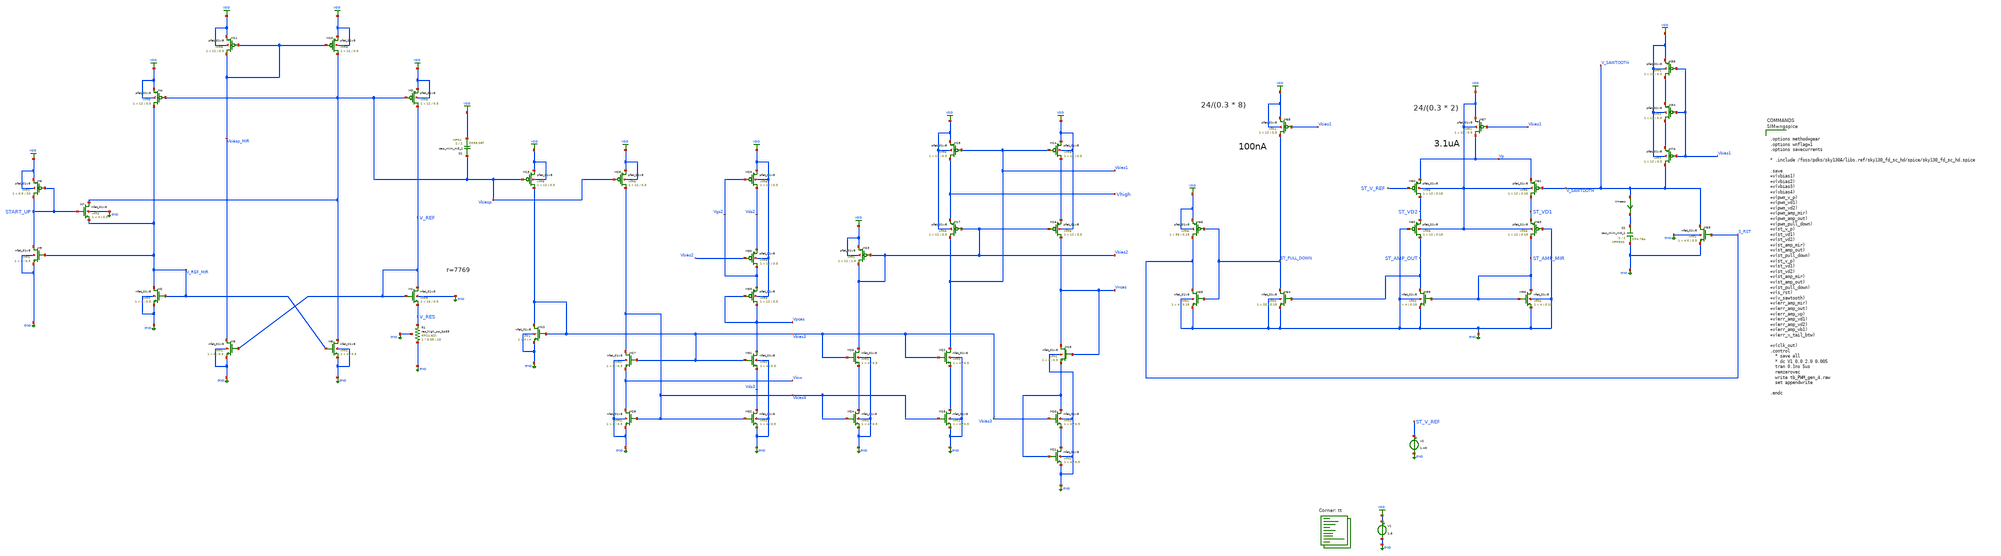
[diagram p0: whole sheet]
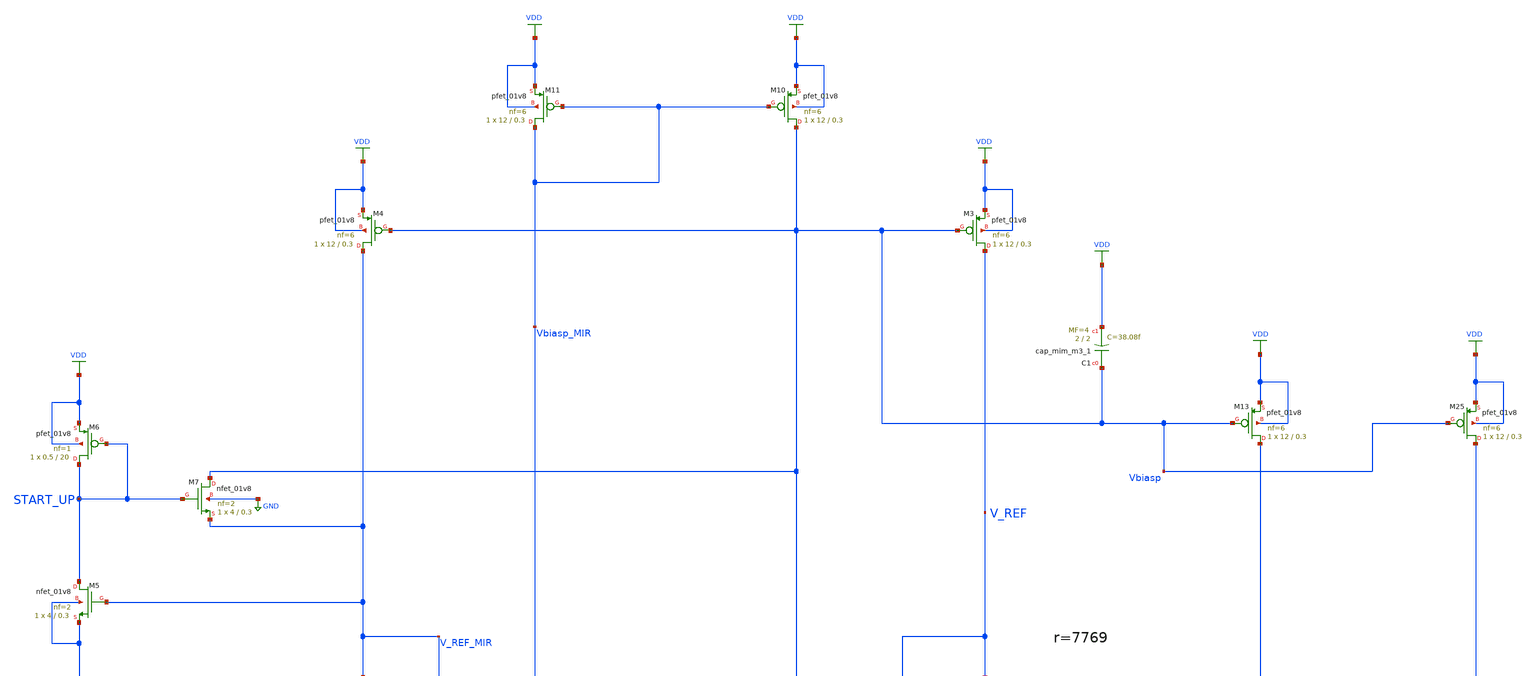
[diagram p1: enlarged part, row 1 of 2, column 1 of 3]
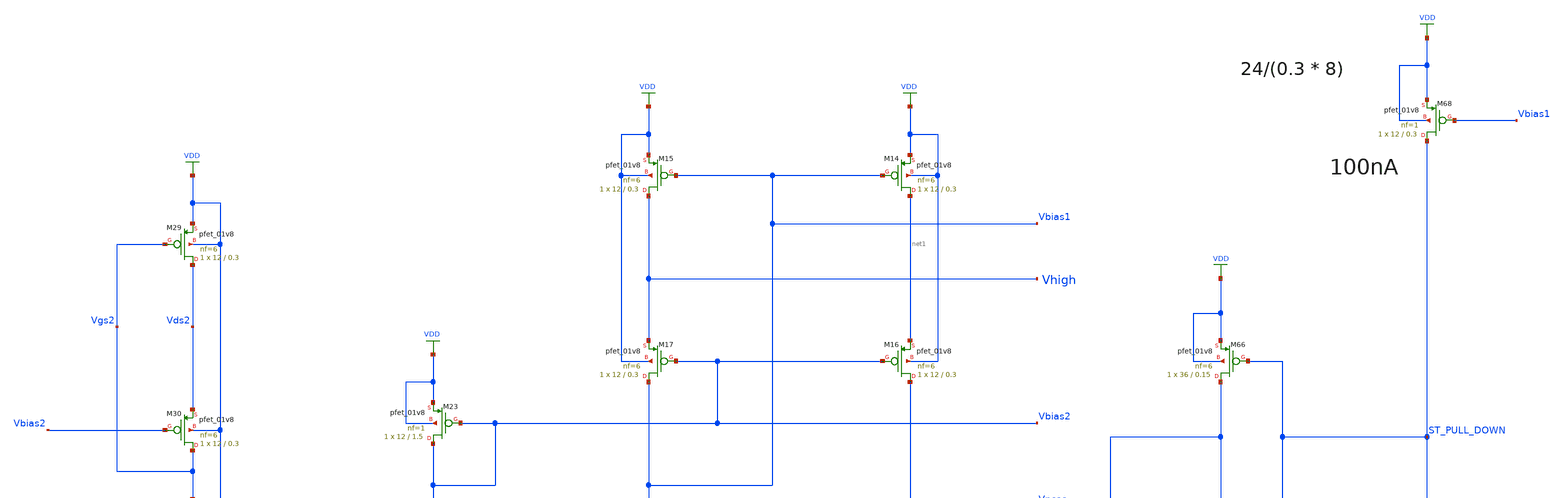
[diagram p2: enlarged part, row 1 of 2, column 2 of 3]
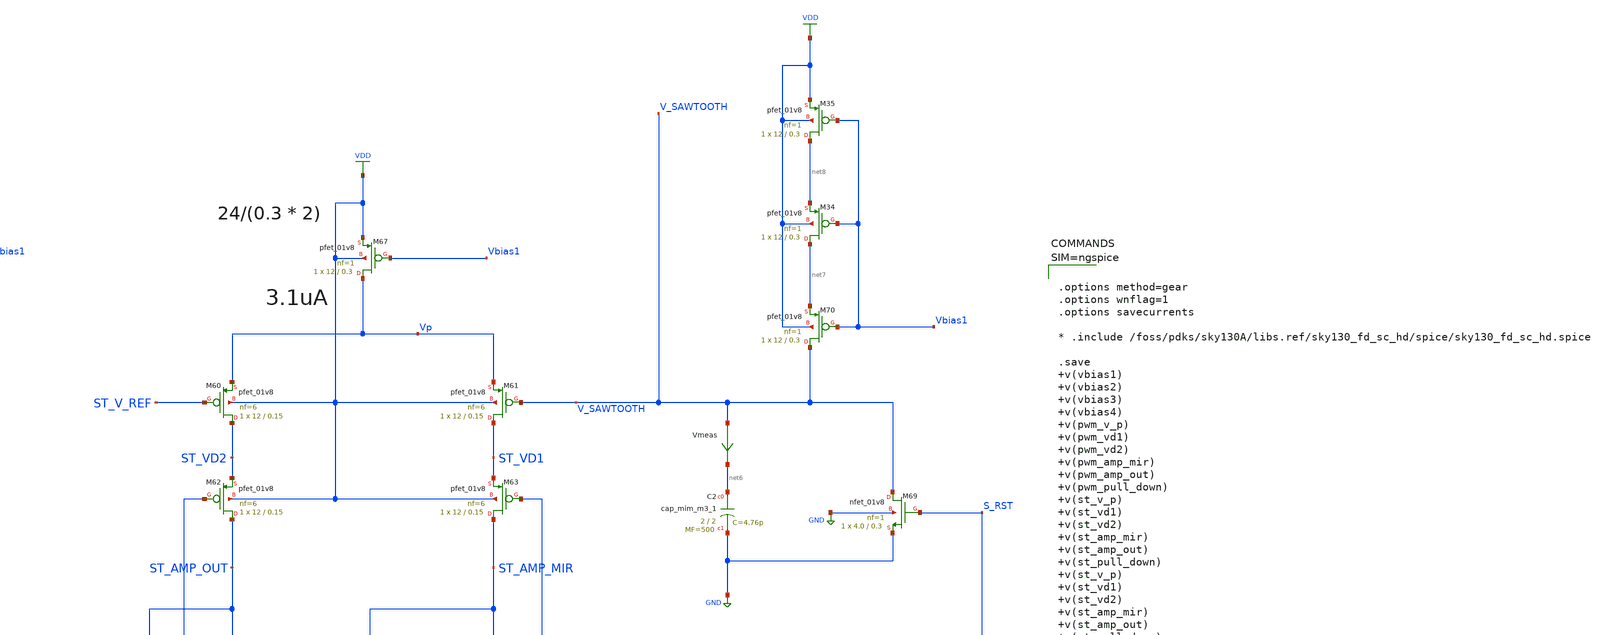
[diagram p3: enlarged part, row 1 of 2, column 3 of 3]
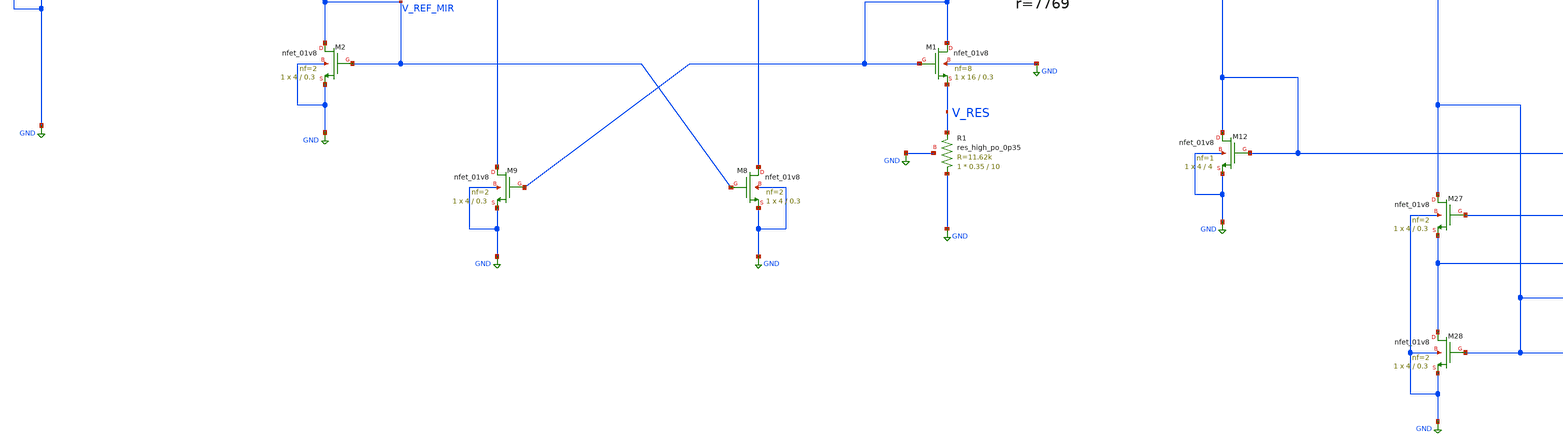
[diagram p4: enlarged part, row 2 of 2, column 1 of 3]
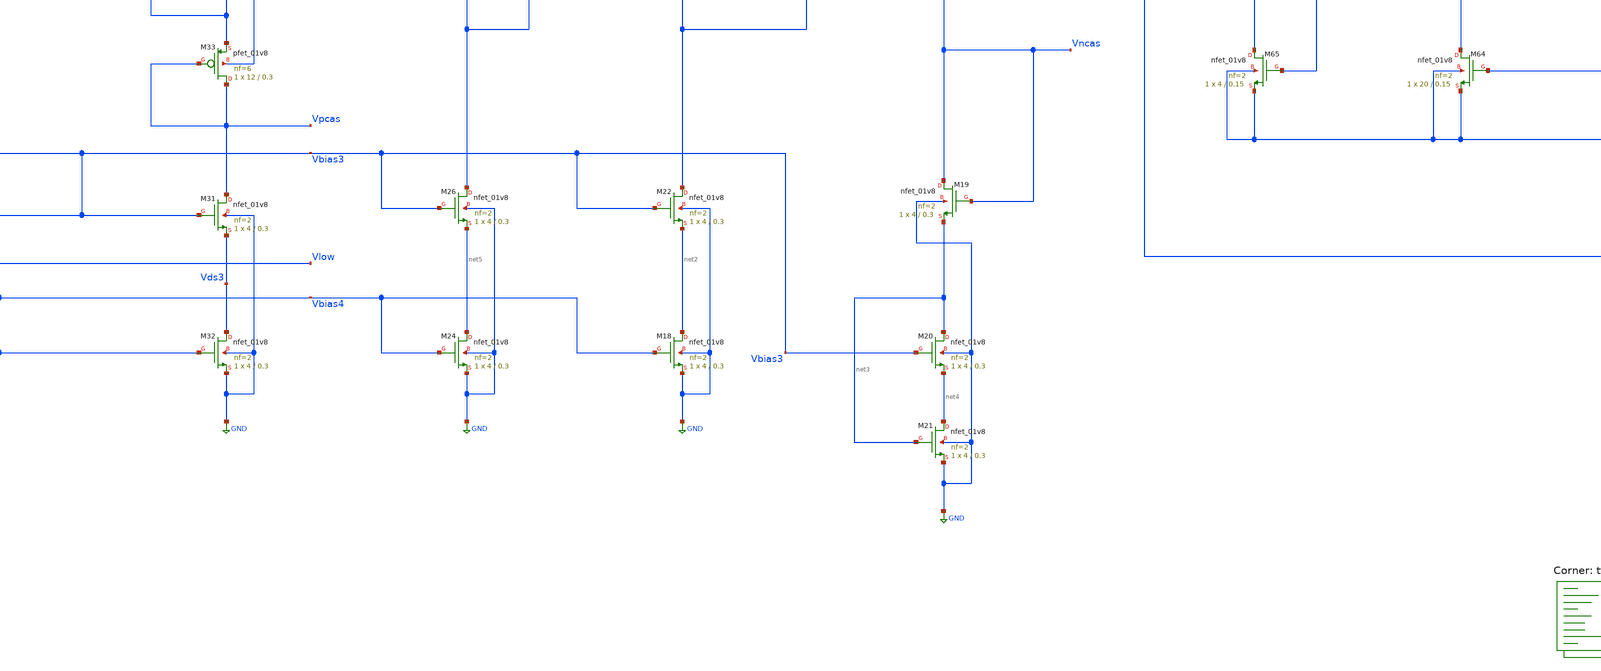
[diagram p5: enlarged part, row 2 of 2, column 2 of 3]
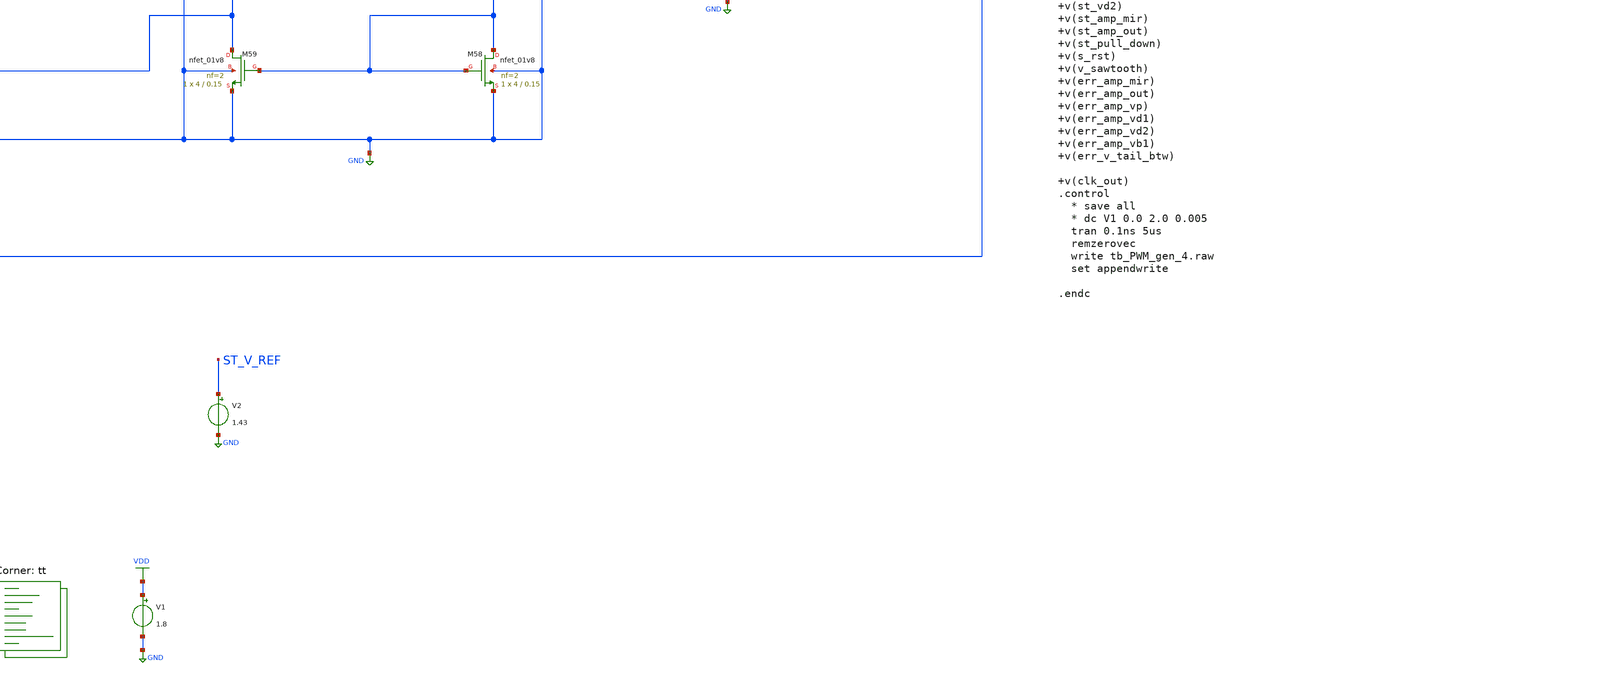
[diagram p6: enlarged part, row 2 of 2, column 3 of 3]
** sch_path: projects/ASU/EEE572/schematic/tb_PWM_gen_4.sch
**.subckt tb_PWM_gen_4
V1 VDD GND 1.8
V2 ST_V_REF GND 1.43
XM1 V_REF V_REF V_RES GND sky130_fd_pr__nfet_01v8 L=0.3 W=16 nf=8 ad='int((nf+1)/2) * W/nf * 0.29' as='int((nf+2)/2) * W/nf * 0.29'
+ pd='2*int((nf+1)/2) * (W/nf + 0.29)' ps='2*int((nf+2)/2) * (W/nf + 0.29)' nrd='0.29 / W' nrs='0.29 / W'
+ sa=0 sb=0 sd=0 mult=1 m=1
XM2 V_REF_MIR V_REF_MIR GND GND sky130_fd_pr__nfet_01v8 L=0.3 W=4 nf=2 ad='int((nf+1)/2) * W/nf * 0.29'
+ as='int((nf+2)/2) * W/nf * 0.29' pd='2*int((nf+1)/2) * (W/nf + 0.29)' ps='2*int((nf+2)/2) * (W/nf + 0.29)'
+ nrd='0.29 / W' nrs='0.29 / W' sa=0 sb=0 sd=0 mult=1 m=1
XM5 START_UP V_REF_MIR GND GND sky130_fd_pr__nfet_01v8 L=0.3 W=4 nf=2 ad='int((nf+1)/2) * W/nf * 0.29'
+ as='int((nf+2)/2) * W/nf * 0.29' pd='2*int((nf+1)/2) * (W/nf + 0.29)' ps='2*int((nf+2)/2) * (W/nf + 0.29)'
+ nrd='0.29 / W' nrs='0.29 / W' sa=0 sb=0 sd=0 mult=1 m=1
XM7 Vbiasp START_UP V_REF_MIR GND sky130_fd_pr__nfet_01v8 L=0.3 W=4 nf=2 ad='int((nf+1)/2) * W/nf * 0.29'
+ as='int((nf+2)/2) * W/nf * 0.29' pd='2*int((nf+1)/2) * (W/nf + 0.29)' ps='2*int((nf+2)/2) * (W/nf + 0.29)'
+ nrd='0.29 / W' nrs='0.29 / W' sa=0 sb=0 sd=0 mult=1 m=1
XM6 START_UP START_UP VDD VDD sky130_fd_pr__pfet_01v8 L=20 W=0.5 nf=1 ad='int((nf+1)/2) * W/nf * 0.29'
+ as='int((nf+2)/2) * W/nf * 0.29' pd='2*int((nf+1)/2) * (W/nf + 0.29)' ps='2*int((nf+2)/2) * (W/nf + 0.29)'
+ nrd='0.29 / W' nrs='0.29 / W' sa=0 sb=0 sd=0 mult=1 m=1
XM3 V_REF Vbiasp VDD VDD sky130_fd_pr__pfet_01v8 L=0.3 W=12 nf=6 ad='int((nf+1)/2) * W/nf * 0.29' as='int((nf+2)/2) * W/nf * 0.29'
+ pd='2*int((nf+1)/2) * (W/nf + 0.29)' ps='2*int((nf+2)/2) * (W/nf + 0.29)' nrd='0.29 / W' nrs='0.29 / W'
+ sa=0 sb=0 sd=0 mult=1 m=1
XM4 V_REF_MIR Vbiasp VDD VDD sky130_fd_pr__pfet_01v8 L=0.3 W=12 nf=6 ad='int((nf+1)/2) * W/nf * 0.29'
+ as='int((nf+2)/2) * W/nf * 0.29' pd='2*int((nf+1)/2) * (W/nf + 0.29)' ps='2*int((nf+2)/2) * (W/nf + 0.29)'
+ nrd='0.29 / W' nrs='0.29 / W' sa=0 sb=0 sd=0 mult=1 m=1
XM8 Vbiasp V_REF_MIR GND GND sky130_fd_pr__nfet_01v8 L=0.3 W=4 nf=2 ad='int((nf+1)/2) * W/nf * 0.29'
+ as='int((nf+2)/2) * W/nf * 0.29' pd='2*int((nf+1)/2) * (W/nf + 0.29)' ps='2*int((nf+2)/2) * (W/nf + 0.29)'
+ nrd='0.29 / W' nrs='0.29 / W' sa=0 sb=0 sd=0 mult=1 m=1
XM9 Vbiasp_MIR V_REF GND GND sky130_fd_pr__nfet_01v8 L=0.3 W=4 nf=2 ad='int((nf+1)/2) * W/nf * 0.29'
+ as='int((nf+2)/2) * W/nf * 0.29' pd='2*int((nf+1)/2) * (W/nf + 0.29)' ps='2*int((nf+2)/2) * (W/nf + 0.29)'
+ nrd='0.29 / W' nrs='0.29 / W' sa=0 sb=0 sd=0 mult=1 m=1
XM10 Vbiasp Vbiasp_MIR VDD VDD sky130_fd_pr__pfet_01v8 L=0.3 W=12 nf=6 ad='int((nf+1)/2) * W/nf * 0.29'
+ as='int((nf+2)/2) * W/nf * 0.29' pd='2*int((nf+1)/2) * (W/nf + 0.29)' ps='2*int((nf+2)/2) * (W/nf + 0.29)'
+ nrd='0.29 / W' nrs='0.29 / W' sa=0 sb=0 sd=0 mult=1 m=1
XM11 Vbiasp_MIR Vbiasp_MIR VDD VDD sky130_fd_pr__pfet_01v8 L=0.3 W=12 nf=6 ad='int((nf+1)/2) * W/nf * 0.29'
+ as='int((nf+2)/2) * W/nf * 0.29' pd='2*int((nf+1)/2) * (W/nf + 0.29)' ps='2*int((nf+2)/2) * (W/nf + 0.29)'
+ nrd='0.29 / W' nrs='0.29 / W' sa=0 sb=0 sd=0 mult=1 m=1
XM12 Vbias3 Vbias3 GND GND sky130_fd_pr__nfet_01v8 L=4 W=4 nf=1 ad='int((nf+1)/2) * W/nf * 0.29' as='int((nf+2)/2) * W/nf * 0.29'
+ pd='2*int((nf+1)/2) * (W/nf + 0.29)' ps='2*int((nf+2)/2) * (W/nf + 0.29)' nrd='0.29 / W' nrs='0.29 / W'
+ sa=0 sb=0 sd=0 mult=1 m=1
XM13 Vbias3 Vbiasp VDD VDD sky130_fd_pr__pfet_01v8 L=0.3 W=12 nf=6 ad='int((nf+1)/2) * W/nf * 0.29' as='int((nf+2)/2) * W/nf * 0.29'
+ pd='2*int((nf+1)/2) * (W/nf + 0.29)' ps='2*int((nf+2)/2) * (W/nf + 0.29)' nrd='0.29 / W' nrs='0.29 / W'
+ sa=0 sb=0 sd=0 mult=1 m=1
XM14 net1 Vbias1 VDD VDD sky130_fd_pr__pfet_01v8 L=0.3 W=12 nf=6 ad='int((nf+1)/2) * W/nf * 0.29' as='int((nf+2)/2) * W/nf * 0.29'
+ pd='2*int((nf+1)/2) * (W/nf + 0.29)' ps='2*int((nf+2)/2) * (W/nf + 0.29)' nrd='0.29 / W' nrs='0.29 / W'
+ sa=0 sb=0 sd=0 mult=1 m=1
XM15 Vhigh Vbias1 VDD VDD sky130_fd_pr__pfet_01v8 L=0.3 W=12 nf=6 ad='int((nf+1)/2) * W/nf * 0.29' as='int((nf+2)/2) * W/nf * 0.29'
+ pd='2*int((nf+1)/2) * (W/nf + 0.29)' ps='2*int((nf+2)/2) * (W/nf + 0.29)' nrd='0.29 / W' nrs='0.29 / W'
+ sa=0 sb=0 sd=0 mult=1 m=1
XM16 Vncas Vbias2 net1 VDD sky130_fd_pr__pfet_01v8 L=0.3 W=12 nf=6 ad='int((nf+1)/2) * W/nf * 0.29' as='int((nf+2)/2) * W/nf * 0.29'
+ pd='2*int((nf+1)/2) * (W/nf + 0.29)' ps='2*int((nf+2)/2) * (W/nf + 0.29)' nrd='0.29 / W' nrs='0.29 / W'
+ sa=0 sb=0 sd=0 mult=1 m=1
XM17 Vbias1 Vbias2 Vhigh VDD sky130_fd_pr__pfet_01v8 L=0.3 W=12 nf=6 ad='int((nf+1)/2) * W/nf * 0.29'
+ as='int((nf+2)/2) * W/nf * 0.29' pd='2*int((nf+1)/2) * (W/nf + 0.29)' ps='2*int((nf+2)/2) * (W/nf + 0.29)'
+ nrd='0.29 / W' nrs='0.29 / W' sa=0 sb=0 sd=0 mult=1 m=1
XM18 net2 Vbias4 GND GND sky130_fd_pr__nfet_01v8 L=0.3 W=4 nf=2 ad='int((nf+1)/2) * W/nf * 0.29' as='int((nf+2)/2) * W/nf * 0.29'
+ pd='2*int((nf+1)/2) * (W/nf + 0.29)' ps='2*int((nf+2)/2) * (W/nf + 0.29)' nrd='0.29 / W' nrs='0.29 / W'
+ sa=0 sb=0 sd=0 mult=1 m=1
XM19 Vncas Vncas net3 GND sky130_fd_pr__nfet_01v8 L=0.3 W=4 nf=2 ad='int((nf+1)/2) * W/nf * 0.29' as='int((nf+2)/2) * W/nf * 0.29'
+ pd='2*int((nf+1)/2) * (W/nf + 0.29)' ps='2*int((nf+2)/2) * (W/nf + 0.29)' nrd='0.29 / W' nrs='0.29 / W'
+ sa=0 sb=0 sd=0 mult=1 m=1
XM20 net3 Vbias3 net4 GND sky130_fd_pr__nfet_01v8 L=0.3 W=4 nf=2 ad='int((nf+1)/2) * W/nf * 0.29' as='int((nf+2)/2) * W/nf * 0.29'
+ pd='2*int((nf+1)/2) * (W/nf + 0.29)' ps='2*int((nf+2)/2) * (W/nf + 0.29)' nrd='0.29 / W' nrs='0.29 / W'
+ sa=0 sb=0 sd=0 mult=1 m=1
XM21 net4 net3 GND GND sky130_fd_pr__nfet_01v8 L=0.3 W=4 nf=2 ad='int((nf+1)/2) * W/nf * 0.29' as='int((nf+2)/2) * W/nf * 0.29'
+ pd='2*int((nf+1)/2) * (W/nf + 0.29)' ps='2*int((nf+2)/2) * (W/nf + 0.29)' nrd='0.29 / W' nrs='0.29 / W'
+ sa=0 sb=0 sd=0 mult=1 m=1
XM25 Vbias4 Vbiasp VDD VDD sky130_fd_pr__pfet_01v8 L=0.3 W=12 nf=6 ad='int((nf+1)/2) * W/nf * 0.29' as='int((nf+2)/2) * W/nf * 0.29'
+ pd='2*int((nf+1)/2) * (W/nf + 0.29)' ps='2*int((nf+2)/2) * (W/nf + 0.29)' nrd='0.29 / W' nrs='0.29 / W'
+ sa=0 sb=0 sd=0 mult=1 m=1
XM27 Vbias4 Vbias3 Vlow GND sky130_fd_pr__nfet_01v8 L=0.3 W=4 nf=2 ad='int((nf+1)/2) * W/nf * 0.29' as='int((nf+2)/2) * W/nf * 0.29'
+ pd='2*int((nf+1)/2) * (W/nf + 0.29)' ps='2*int((nf+2)/2) * (W/nf + 0.29)' nrd='0.29 / W' nrs='0.29 / W'
+ sa=0 sb=0 sd=0 mult=1 m=1
XM28 Vlow Vbias4 GND GND sky130_fd_pr__nfet_01v8 L=0.3 W=4 nf=2 ad='int((nf+1)/2) * W/nf * 0.29' as='int((nf+2)/2) * W/nf * 0.29'
+ pd='2*int((nf+1)/2) * (W/nf + 0.29)' ps='2*int((nf+2)/2) * (W/nf + 0.29)' nrd='0.29 / W' nrs='0.29 / W'
+ sa=0 sb=0 sd=0 mult=1 m=1
XM29 Vds2 Vgs2 VDD VDD sky130_fd_pr__pfet_01v8 L=0.3 W=12 nf=6 ad='int((nf+1)/2) * W/nf * 0.29' as='int((nf+2)/2) * W/nf * 0.29'
+ pd='2*int((nf+1)/2) * (W/nf + 0.29)' ps='2*int((nf+2)/2) * (W/nf + 0.29)' nrd='0.29 / W' nrs='0.29 / W'
+ sa=0 sb=0 sd=0 mult=1 m=1
XM30 Vgs2 Vbias2 Vds2 VDD sky130_fd_pr__pfet_01v8 L=0.3 W=12 nf=6 ad='int((nf+1)/2) * W/nf * 0.29' as='int((nf+2)/2) * W/nf * 0.29'
+ pd='2*int((nf+1)/2) * (W/nf + 0.29)' ps='2*int((nf+2)/2) * (W/nf + 0.29)' nrd='0.29 / W' nrs='0.29 / W'
+ sa=0 sb=0 sd=0 mult=1 m=1
XM31 Vpcas Vbias3 Vds3 GND sky130_fd_pr__nfet_01v8 L=0.3 W=4 nf=2 ad='int((nf+1)/2) * W/nf * 0.29' as='int((nf+2)/2) * W/nf * 0.29'
+ pd='2*int((nf+1)/2) * (W/nf + 0.29)' ps='2*int((nf+2)/2) * (W/nf + 0.29)' nrd='0.29 / W' nrs='0.29 / W'
+ sa=0 sb=0 sd=0 mult=1 m=1
XM32 Vds3 Vbias4 GND GND sky130_fd_pr__nfet_01v8 L=0.3 W=4 nf=2 ad='int((nf+1)/2) * W/nf * 0.29' as='int((nf+2)/2) * W/nf * 0.29'
+ pd='2*int((nf+1)/2) * (W/nf + 0.29)' ps='2*int((nf+2)/2) * (W/nf + 0.29)' nrd='0.29 / W' nrs='0.29 / W'
+ sa=0 sb=0 sd=0 mult=1 m=1
XM33 Vpcas Vpcas Vgs2 VDD sky130_fd_pr__pfet_01v8 L=0.3 W=12 nf=6 ad='int((nf+1)/2) * W/nf * 0.29' as='int((nf+2)/2) * W/nf * 0.29'
+ pd='2*int((nf+1)/2) * (W/nf + 0.29)' ps='2*int((nf+2)/2) * (W/nf + 0.29)' nrd='0.29 / W' nrs='0.29 / W'
+ sa=0 sb=0 sd=0 mult=1 m=1
XM22 Vbias1 Vbias3 net2 GND sky130_fd_pr__nfet_01v8 L=0.3 W=4 nf=2 ad='int((nf+1)/2) * W/nf * 0.29' as='int((nf+2)/2) * W/nf * 0.29'
+ pd='2*int((nf+1)/2) * (W/nf + 0.29)' ps='2*int((nf+2)/2) * (W/nf + 0.29)' nrd='0.29 / W' nrs='0.29 / W'
+ sa=0 sb=0 sd=0 mult=1 m=1
XM23 Vbias2 Vbias2 VDD VDD sky130_fd_pr__pfet_01v8 L=1.5 W=12 nf=1 ad='int((nf+1)/2) * W/nf * 0.29' as='int((nf+2)/2) * W/nf * 0.29'
+ pd='2*int((nf+1)/2) * (W/nf + 0.29)' ps='2*int((nf+2)/2) * (W/nf + 0.29)' nrd='0.29 / W' nrs='0.29 / W'
+ sa=0 sb=0 sd=0 mult=1 m=1
XM24 net5 Vbias4 GND GND sky130_fd_pr__nfet_01v8 L=0.3 W=4 nf=2 ad='int((nf+1)/2) * W/nf * 0.29' as='int((nf+2)/2) * W/nf * 0.29'
+ pd='2*int((nf+1)/2) * (W/nf + 0.29)' ps='2*int((nf+2)/2) * (W/nf + 0.29)' nrd='0.29 / W' nrs='0.29 / W'
+ sa=0 sb=0 sd=0 mult=1 m=1
XM26 Vbias2 Vbias3 net5 GND sky130_fd_pr__nfet_01v8 L=0.3 W=4 nf=2 ad='int((nf+1)/2) * W/nf * 0.29' as='int((nf+2)/2) * W/nf * 0.29'
+ pd='2*int((nf+1)/2) * (W/nf + 0.29)' ps='2*int((nf+2)/2) * (W/nf + 0.29)' nrd='0.29 / W' nrs='0.29 / W'
+ sa=0 sb=0 sd=0 mult=1 m=1
XC1 Vbiasp VDD sky130_fd_pr__cap_mim_m3_1 W=2 L=2 MF=4 m=4
XR1 GND V_RES GND sky130_fd_pr__res_high_po_0p35 L=10 mult=1 m=1
XM58 ST_AMP_MIR ST_AMP_MIR GND GND sky130_fd_pr__nfet_01v8 L=0.15 W=4 nf=2 ad='int((nf+1)/2) * W/nf * 0.29'
+ as='int((nf+2)/2) * W/nf * 0.29' pd='2*int((nf+1)/2) * (W/nf + 0.29)' ps='2*int((nf+2)/2) * (W/nf + 0.29)'
+ nrd='0.29 / W' nrs='0.29 / W' sa=0 sb=0 sd=0 mult=1 m=1
XM59 ST_AMP_OUT ST_AMP_MIR GND GND sky130_fd_pr__nfet_01v8 L=0.15 W=4 nf=2 ad='int((nf+1)/2) * W/nf * 0.29'
+ as='int((nf+2)/2) * W/nf * 0.29' pd='2*int((nf+1)/2) * (W/nf + 0.29)' ps='2*int((nf+2)/2) * (W/nf + 0.29)'
+ nrd='0.29 / W' nrs='0.29 / W' sa=0 sb=0 sd=0 mult=1 m=1
XM60 ST_VD2 ST_V_REF Vp VDD sky130_fd_pr__pfet_01v8 L=0.15 W=12 nf=6 ad='int((nf+1)/2) * W/nf * 0.29'
+ as='int((nf+2)/2) * W/nf * 0.29' pd='2*int((nf+1)/2) * (W/nf + 0.29)' ps='2*int((nf+2)/2) * (W/nf + 0.29)'
+ nrd='0.29 / W' nrs='0.29 / W' sa=0 sb=0 sd=0 mult=1 m=1
XM61 ST_VD1 V_SAWTOOTH Vp VDD sky130_fd_pr__pfet_01v8 L=0.15 W=12 nf=6 ad='int((nf+1)/2) * W/nf * 0.29'
+ as='int((nf+2)/2) * W/nf * 0.29' pd='2*int((nf+1)/2) * (W/nf + 0.29)' ps='2*int((nf+2)/2) * (W/nf + 0.29)'
+ nrd='0.29 / W' nrs='0.29 / W' sa=0 sb=0 sd=0 mult=1 m=1
XM62 ST_AMP_OUT GND ST_VD2 VDD sky130_fd_pr__pfet_01v8 L=0.15 W=12 nf=6 ad='int((nf+1)/2) * W/nf * 0.29'
+ as='int((nf+2)/2) * W/nf * 0.29' pd='2*int((nf+1)/2) * (W/nf + 0.29)' ps='2*int((nf+2)/2) * (W/nf + 0.29)'
+ nrd='0.29 / W' nrs='0.29 / W' sa=0 sb=0 sd=0 mult=1 m=1
XM63 ST_AMP_MIR GND ST_VD1 VDD sky130_fd_pr__pfet_01v8 L=0.15 W=12 nf=6 ad='int((nf+1)/2) * W/nf * 0.29'
+ as='int((nf+2)/2) * W/nf * 0.29' pd='2*int((nf+1)/2) * (W/nf + 0.29)' ps='2*int((nf+2)/2) * (W/nf + 0.29)'
+ nrd='0.29 / W' nrs='0.29 / W' sa=0 sb=0 sd=0 mult=1 m=1
XM64 ST_PULL_DOWN ST_AMP_OUT GND GND sky130_fd_pr__nfet_01v8 L=0.15 W=20 nf=2 ad='int((nf+1)/2) * W/nf * 0.29'
+ as='int((nf+2)/2) * W/nf * 0.29' pd='2*int((nf+1)/2) * (W/nf + 0.29)' ps='2*int((nf+2)/2) * (W/nf + 0.29)'
+ nrd='0.29 / W' nrs='0.29 / W' sa=0 sb=0 sd=0 mult=1 m=1
XM65 S_RST ST_PULL_DOWN GND GND sky130_fd_pr__nfet_01v8 L=0.15 W=4 nf=2 ad='int((nf+1)/2) * W/nf * 0.29'
+ as='int((nf+2)/2) * W/nf * 0.29' pd='2*int((nf+1)/2) * (W/nf + 0.29)' ps='2*int((nf+2)/2) * (W/nf + 0.29)'
+ nrd='0.29 / W' nrs='0.29 / W' sa=0 sb=0 sd=0 mult=1 m=1
XM66 S_RST ST_PULL_DOWN VDD VDD sky130_fd_pr__pfet_01v8 L=0.15 W=36 nf=6 ad='int((nf+1)/2) * W/nf * 0.29'
+ as='int((nf+2)/2) * W/nf * 0.29' pd='2*int((nf+1)/2) * (W/nf + 0.29)' ps='2*int((nf+2)/2) * (W/nf + 0.29)'
+ nrd='0.29 / W' nrs='0.29 / W' sa=0 sb=0 sd=0 mult=1 m=1
XM67 Vp Vbias1 VDD VDD sky130_fd_pr__pfet_01v8 L=0.3 W=12 nf=1 ad='int((nf+1)/2) * W/nf * 0.29' as='int((nf+2)/2) * W/nf * 0.29'
+ pd='2*int((nf+1)/2) * (W/nf + 0.29)' ps='2*int((nf+2)/2) * (W/nf + 0.29)' nrd='0.29 / W' nrs='0.29 / W'
+ sa=0 sb=0 sd=0 mult=1 m=1
XM68 ST_PULL_DOWN Vbias1 VDD VDD sky130_fd_pr__pfet_01v8 L=0.3 W=12 nf=1 ad='int((nf+1)/2) * W/nf * 0.29'
+ as='int((nf+2)/2) * W/nf * 0.29' pd='2*int((nf+1)/2) * (W/nf + 0.29)' ps='2*int((nf+2)/2) * (W/nf + 0.29)'
+ nrd='0.29 / W' nrs='0.29 / W' sa=0 sb=0 sd=0 mult=1 m=1
XC2 net6 GND sky130_fd_pr__cap_mim_m3_1 W=2 L=2 MF=500 m=500
Vmeas V_SAWTOOTH net6 0
.save i(vmeas)
XM69 V_SAWTOOTH S_RST GND GND sky130_fd_pr__nfet_01v8 L=0.3 W=4.0 nf=1 ad='int((nf+1)/2) * W/nf * 0.29'
+ as='int((nf+2)/2) * W/nf * 0.29' pd='2*int((nf+1)/2) * (W/nf + 0.29)' ps='2*int((nf+2)/2) * (W/nf + 0.29)'
+ nrd='0.29 / W' nrs='0.29 / W' sa=0 sb=0 sd=0 mult=1 m=1
XM70 V_SAWTOOTH Vbias1 net7 VDD sky130_fd_pr__pfet_01v8 L=0.3 W=12 nf=1 ad='int((nf+1)/2) * W/nf * 0.29'
+ as='int((nf+2)/2) * W/nf * 0.29' pd='2*int((nf+1)/2) * (W/nf + 0.29)' ps='2*int((nf+2)/2) * (W/nf + 0.29)'
+ nrd='0.29 / W' nrs='0.29 / W' sa=0 sb=0 sd=0 mult=1 m=1
XM34 net7 Vbias1 net8 VDD sky130_fd_pr__pfet_01v8 L=0.3 W=12 nf=1 ad='int((nf+1)/2) * W/nf * 0.29' as='int((nf+2)/2) * W/nf * 0.29'
+ pd='2*int((nf+1)/2) * (W/nf + 0.29)' ps='2*int((nf+2)/2) * (W/nf + 0.29)' nrd='0.29 / W' nrs='0.29 / W'
+ sa=0 sb=0 sd=0 mult=1 m=1
XM35 net8 Vbias1 VDD VDD sky130_fd_pr__pfet_01v8 L=0.3 W=12 nf=1 ad='int((nf+1)/2) * W/nf * 0.29' as='int((nf+2)/2) * W/nf * 0.29'
+ pd='2*int((nf+1)/2) * (W/nf + 0.29)' ps='2*int((nf+2)/2) * (W/nf + 0.29)' nrd='0.29 / W' nrs='0.29 / W'
+ sa=0 sb=0 sd=0 mult=1 m=1
**** begin user architecture code
.lib $::SKYWATER_MODELS/sky130.lib.spice tt



.options method=gear
.options wnflag=1
.options savecurrents

* .include /foss/pdks/sky130A/libs.ref/sky130_fd_sc_hd/spice/sky130_fd_sc_hd.spice

.save v(vbias1) v(vbias2) v(vbias3) v(vbias4) v(pwm_v_p) v(pwm_vd1) v(pwm_vd2) v(pwm_amp_mir) v(pwm_amp_out) v(pwm_pull_down) v(st_v_p) v(st_vd1) v(st_vd2) v(st_amp_mir) v(st_amp_out) v(st_pull_down) v(st_v_p) v(st_vd1) v(st_vd2) v(st_amp_mir) v(st_amp_out) v(st_pull_down) v(s_rst) v(v_sawtooth) v(err_amp_mir) v(err_amp_out) v(err_amp_vp) v(err_amp_vd1) v(err_amp_vd2) v(err_amp_vb1) v(err_v_tail_btw)
 v(clk_out)
.control
  * save all
  * dc V1 0.0 2.0 0.005
  tran 0.1ns 5us
  remzerovec
  write tb_PWM_gen_4.raw
  set appendwrite

.endc





**** end user architecture code
**.ends
.GLOBAL GND
.GLOBAL VDD
.end
